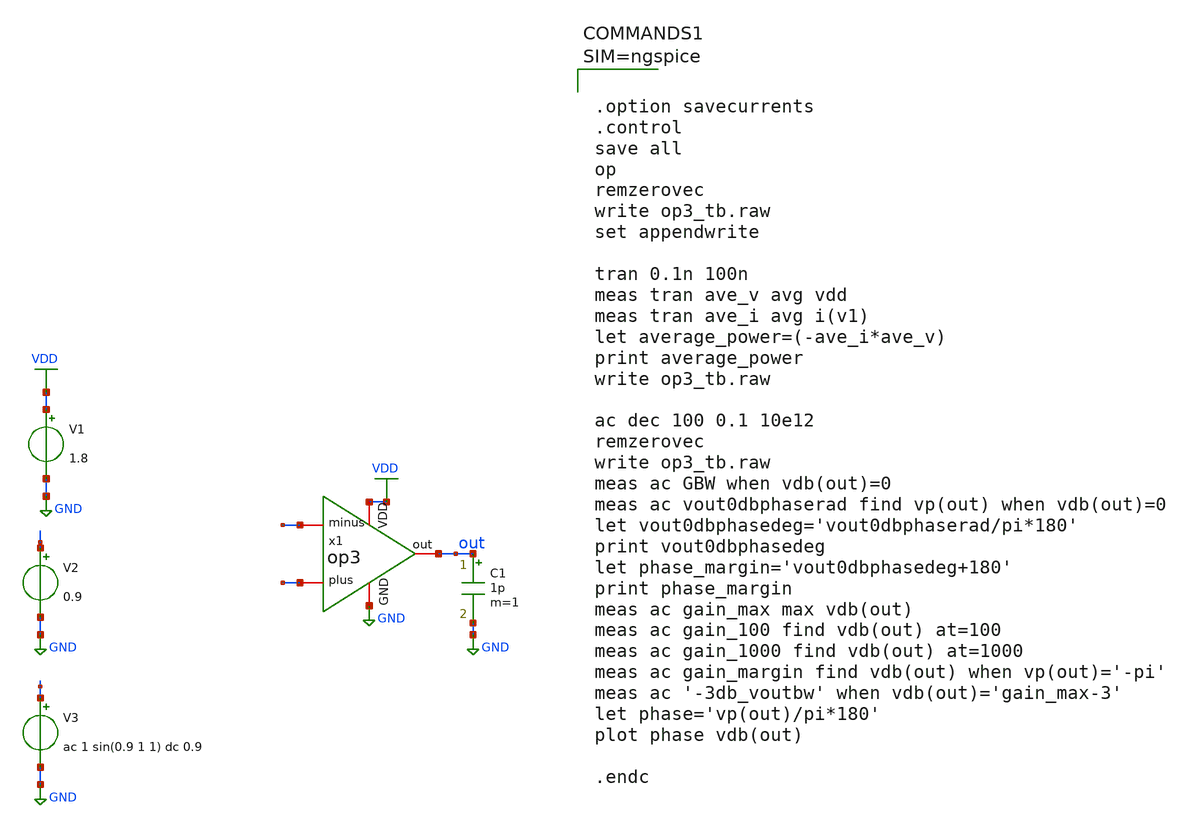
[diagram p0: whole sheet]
** sch_path: xschem/op3_tb.sch
**.subckt op3_tb
V1 VDD GND 1.8
V2 + GND 0.9
V3 - GND ac 1 sin(0.9 1 1) dc 0.9
C1 out GND 1p m=1
x1 VDD out - + GND op3
**** begin user architecture code

** opencircuitdesign pdks install
.lib $::SKYWATER_MODELS/sky130.lib.spice tt





.option savecurrents
.control
save all
op
remzerovec
write op3_tb.raw
set appendwrite

tran 0.1n 100n
meas tran ave_v avg vdd
meas tran ave_i avg i(v1)
let average_power=(-ave_i*ave_v)
print average_power
write op3_tb.raw

ac dec 100 0.1 10e12
remzerovec
write op3_tb.raw
meas ac GBW when vdb(out)=0
meas ac vout0dbphaserad find vp(out) when vdb(out)=0
let vout0dbphasedeg='vout0dbphaserad/pi*180'
print vout0dbphasedeg
let phase_margin='vout0dbphasedeg+180'
print phase_margin
meas ac gain_max max vdb(out)
meas ac gain_100 find vdb(out) at=100
meas ac gain_1000 find vdb(out) at=1000
meas ac gain_margin find vdb(out) when vp(out)='-pi'
meas ac '-3db_voutbw' when vdb(out)='gain_max-3'
let phase='vp(out)/pi*180'
plot phase vdb(out)

.endc



**** end user architecture code
**.ends

* expanding   symbol:  op3.sym # of pins=5
** sym_path: xschem/op3.sym
** sch_path: xschem/op3.sch
.subckt op3 VDD out minus plus GND
*.iopin VDD
*.iopin GND
*.iopin minus
*.iopin plus
*.iopin out
**** begin user architecture code


**diffpair**
.param L1=1
.param W1=5
.param M1=1

**PMOS**
.param L2=1
.param W2=2
.param M2=1

**NMOS**
.param L3=10
.param W3=1
.param M3=1

**Current control**
.param L4=5
.param W4=2.5
.param M4=1


**** end user architecture code
V4 bias GND dc 0.6
XM1 net2 minus net1 GND sky130_fd_pr__nfet_01v8 L={L1} W={W1} nf=1 ad='int((nf+1)/2) * W/nf * 0.29' as='int((nf+2)/2) * W/nf * 0.29'
+ pd='2*int((nf+1)/2) * (W/nf + 0.29)' ps='2*int((nf+2)/2) * (W/nf + 0.29)' nrd='0.29 / W' nrs='0.29 / W'
+ sa=0 sb=0 sd=0 mult={M1} m={M1}
XM3 net8 bias GND GND sky130_fd_pr__nfet_01v8 L={L4} W={W4} nf=1 ad='int((nf+1)/2) * W/nf * 0.29' as='int((nf+2)/2) * W/nf * 0.29'
+ pd='2*int((nf+1)/2) * (W/nf + 0.29)' ps='2*int((nf+2)/2) * (W/nf + 0.29)' nrd='0.29 / W' nrs='0.29 / W'
+ sa=0 sb=0 sd=0 mult={M4} m={M4}
Vbias net1 net8 0
.save i(vbias)
XM2 net4 plus net1 GND sky130_fd_pr__nfet_01v8 L={L1} W={W1} nf=1 ad='int((nf+1)/2) * W/nf * 0.29' as='int((nf+2)/2) * W/nf * 0.29'
+ pd='2*int((nf+1)/2) * (W/nf + 0.29)' ps='2*int((nf+2)/2) * (W/nf + 0.29)' nrd='0.29 / W' nrs='0.29 / W'
+ sa=0 sb=0 sd=0 mult={M1} m={M1}
XM7 net5 bias2 net2 VDD sky130_fd_pr__pfet_01v8 L={L3} W={W3} nf=1 ad='int((nf+1)/2) * W/nf * 0.29' as='int((nf+2)/2) * W/nf * 0.29'
+ pd='2*int((nf+1)/2) * (W/nf + 0.29)' ps='2*int((nf+2)/2) * (W/nf + 0.29)' nrd='0.29 / W' nrs='0.29 / W'
+ sa=0 sb=0 sd=0 mult={M3} m={M3}
XM8 net5 bias3 net6 GND sky130_fd_pr__nfet_01v8 L={L2} W={W2} nf=1 ad='int((nf+1)/2) * W/nf * 0.29' as='int((nf+2)/2) * W/nf * 0.29'
+ pd='2*int((nf+1)/2) * (W/nf + 0.29)' ps='2*int((nf+2)/2) * (W/nf + 0.29)' nrd='0.29 / W' nrs='0.29 / W'
+ sa=0 sb=0 sd=0 mult={M2} m={M2}
XM9 net6 net5 GND GND sky130_fd_pr__nfet_01v8 L={L2} W={W2} nf=1 ad='int((nf+1)/2) * W/nf * 0.29' as='int((nf+2)/2) * W/nf * 0.29'
+ pd='2*int((nf+1)/2) * (W/nf + 0.29)' ps='2*int((nf+2)/2) * (W/nf + 0.29)' nrd='0.29 / W' nrs='0.29 / W'
+ sa=0 sb=0 sd=0 mult={M2} m={M2}
XM10 out bias3 net7 GND sky130_fd_pr__nfet_01v8 L={L2} W={W2} nf=1 ad='int((nf+1)/2) * W/nf * 0.29' as='int((nf+2)/2) * W/nf * 0.29'
+ pd='2*int((nf+1)/2) * (W/nf + 0.29)' ps='2*int((nf+2)/2) * (W/nf + 0.29)' nrd='0.29 / W' nrs='0.29 / W'
+ sa=0 sb=0 sd=0 mult={M2} m={M2}
XM11 net7 net5 GND GND sky130_fd_pr__nfet_01v8 L={L2} W={W2} nf=1 ad='int((nf+1)/2) * W/nf * 0.29' as='int((nf+2)/2) * W/nf * 0.29'
+ pd='2*int((nf+1)/2) * (W/nf + 0.29)' ps='2*int((nf+2)/2) * (W/nf + 0.29)' nrd='0.29 / W' nrs='0.29 / W'
+ sa=0 sb=0 sd=0 mult={M2} m={M2}
V5 bias1 GND dc 0.6
V6 bias2 GND dc 0.6
V7 bias3 GND dc 0.6
Vbias1 net3 net4 0
.save i(vbias1)
Vbias2 net9 out 0
.save i(vbias2)
XM4 net2 bias1 VDD VDD sky130_fd_pr__pfet_01v8 L={L3} W={W3} nf=1 ad='int((nf+1)/2) * W/nf * 0.29' as='int((nf+2)/2) * W/nf * 0.29'
+ pd='2*int((nf+1)/2) * (W/nf + 0.29)' ps='2*int((nf+2)/2) * (W/nf + 0.29)' nrd='0.29 / W' nrs='0.29 / W'
+ sa=0 sb=0 sd=0 mult={M3} m={M3}
XM5 net9 bias2 net4 VDD sky130_fd_pr__pfet_01v8 L={L3} W={W3} nf=1 ad='int((nf+1)/2) * W/nf * 0.29' as='int((nf+2)/2) * W/nf * 0.29'
+ pd='2*int((nf+1)/2) * (W/nf + 0.29)' ps='2*int((nf+2)/2) * (W/nf + 0.29)' nrd='0.29 / W' nrs='0.29 / W'
+ sa=0 sb=0 sd=0 mult={M3} m={M3}
XM6 net3 bias1 VDD VDD sky130_fd_pr__pfet_01v8 L={L3} W={W3} nf=1 ad='int((nf+1)/2) * W/nf * 0.29' as='int((nf+2)/2) * W/nf * 0.29'
+ pd='2*int((nf+1)/2) * (W/nf + 0.29)' ps='2*int((nf+2)/2) * (W/nf + 0.29)' nrd='0.29 / W' nrs='0.29 / W'
+ sa=0 sb=0 sd=0 mult={M3} m={M3}
.ends

.GLOBAL VDD
.GLOBAL GND
.end
